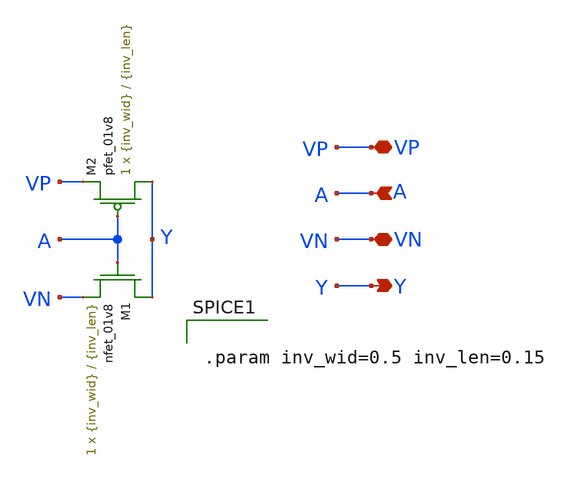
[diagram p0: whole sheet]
** sch_path: LDS/LDS_inverter.sch
**.subckt LDS_inverter VP A Y VN
*.iopin VP
*.ipin A
*.opin Y
*.iopin VN
XM2 Y A VP VP sky130_fd_pr__pfet_01v8 L={inv_len} W={inv_wid} nf=1 ad='int((nf+1)/2) * W/nf * 0.29' as='int((nf+2)/2) * W/nf * 0.29'
+ pd='2*int((nf+1)/2) * (W/nf + 0.29)' ps='2*int((nf+2)/2) * (W/nf + 0.29)' nrd='0.29 / W' nrs='0.29 / W'
+ sa=0 sb=0 sd=0 mult=1 m=1
XM1 Y A VN VN sky130_fd_pr__nfet_01v8 L={inv_len} W={inv_wid} nf=1 ad='int((nf+1)/2) * W/nf * 0.29' as='int((nf+2)/2) * W/nf * 0.29'
+ pd='2*int((nf+1)/2) * (W/nf + 0.29)' ps='2*int((nf+2)/2) * (W/nf + 0.29)' nrd='0.29 / W' nrs='0.29 / W'
+ sa=0 sb=0 sd=0 mult=1 m=1
**** begin user architecture code


.param inv_wid=0.5 inv_len=0.15


**** end user architecture code
**.ends
.end
